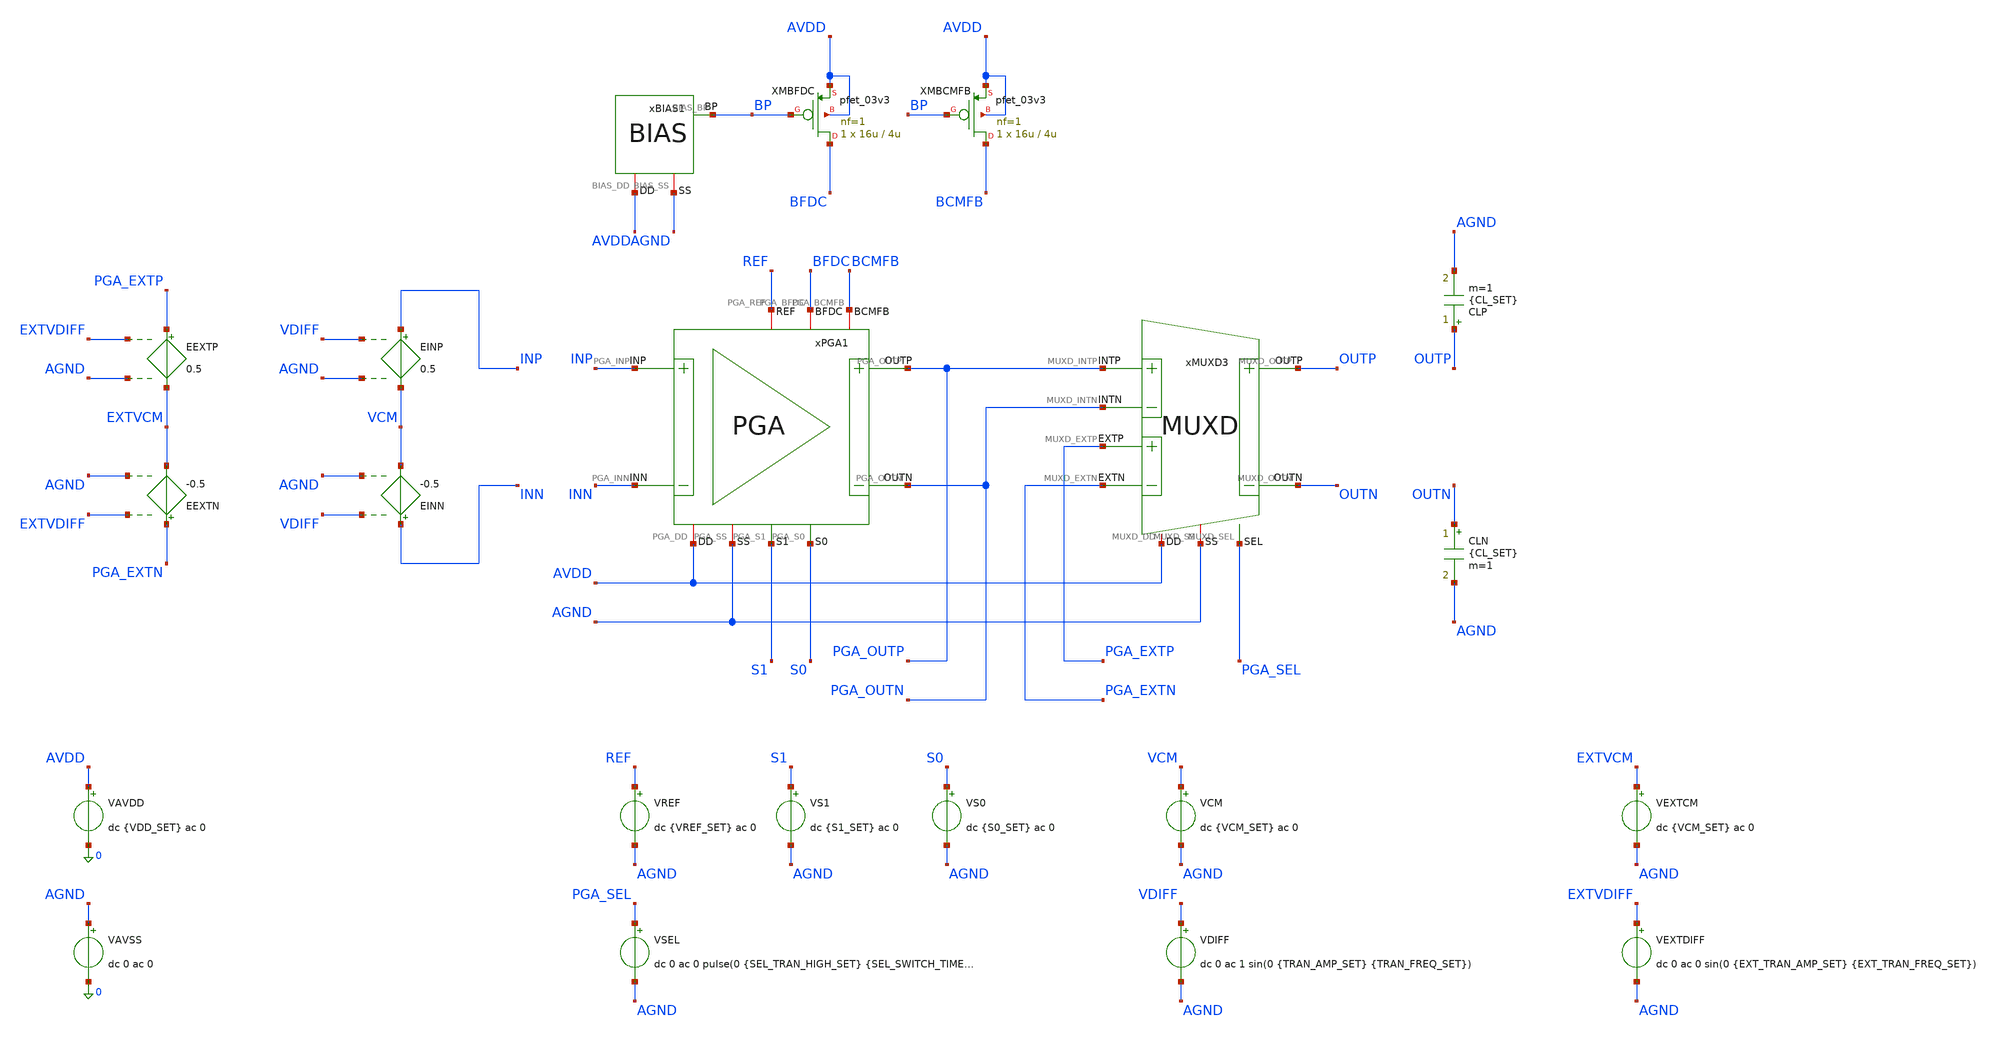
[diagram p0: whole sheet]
** sch_path: Design_Files/IC Design/Testbench/AFE_BLOCKS/PGA/PGA_TB_PVT_NOM.sch
**.subckt PGA_TB_PVT_NOM
CLP OUTP AGND {CL_SET} m=1
CLN OUTN AGND {CL_SET} m=1
xBIAS1 AVDD AGND BP BIAS
XMBFDC BFDC BP AVDD AVDD pfet_03v3 L=4u W=16u nf=1 ad='int((nf+1)/2) * W/nf * 0.18u' as='int((nf+2)/2) * W/nf * 0.18u'
+ pd='2*int((nf+1)/2) * (W/nf + 0.18u)' ps='2*int((nf+2)/2) * (W/nf + 0.18u)' nrd='0.18u / W' nrs='0.18u / W'
+ sa=0 sb=0 sd=0 m=1
XMBCMFB BCMFB BP AVDD AVDD pfet_03v3 L=4u W=16u nf=1 ad='int((nf+1)/2) * W/nf * 0.18u' as='int((nf+2)/2) * W/nf * 0.18u'
+ pd='2*int((nf+1)/2) * (W/nf + 0.18u)' ps='2*int((nf+2)/2) * (W/nf + 0.18u)' nrd='0.18u / W' nrs='0.18u / W'
+ sa=0 sb=0 sd=0 m=1
VAVDD AVDD 0 dc {VDD_SET} ac 0
.save i(vavdd)
VAVSS AGND 0 dc 0 ac 0
VCM VCM AGND dc {VCM_SET} ac 0
VDIFF VDIFF AGND dc 0 ac 1 sin(0 {TRAN_AMP_SET} {TRAN_FREQ_SET})
VREF REF AGND dc {VREF_SET} ac 0
VSEL PGA_SEL AGND dc 0 ac 0 pulse(0 {SEL_TRAN_HIGH_SET} {SEL_SWITCH_TIME_SET} 1u 1u 400m 800m)
VEXTCM EXTVCM AGND dc {VCM_SET} ac 0
VEXTDIFF EXTVDIFF AGND dc 0 ac 0 sin(0 {EXT_TRAN_AMP_SET} {EXT_TRAN_FREQ_SET})
EINP INP VCM VDIFF AGND 0.5
EINN INN VCM VDIFF AGND -0.5
EEXTP PGA_EXTP EXTVCM EXTVDIFF AGND 0.5
EEXTN PGA_EXTN EXTVCM EXTVDIFF AGND -0.5
xPGA1 AVDD AGND INP INN PGA_OUTN BFDC PGA_OUTP BCMFB REF S1 S0 PGA
xMUXD3 AVDD AGND PGA_OUTP PGA_OUTN OUTN OUTP PGA_EXTP PGA_EXTN PGA_SEL MUXD
VS1 S1 AGND dc {S1_SET} ac 0
VS0 S0 AGND dc {S0_SET} ac 0
**** begin user architecture code

* {MODELS_START}
.include $::180MCU_MODELS/design.ngspice

.param sw_stat_global=0
.param sw_stat_mismatch=0

.lib $::180MCU_MODELS/sm141064.ngspice typical
.lib $::180MCU_MODELS/sm141064.ngspice res_typical
.lib $::180MCU_MODELS/sm141064.ngspice mimcap_typical
.lib $::180MCU_MODELS/sm141064.ngspice cap_mim
.lib $::180MCU_MODELS/sm141064.ngspice bjt_typical

.csparam PROC_ID=0
* {MODELS_END}



* {SETUP_START}
.param VDD_SET=3.3
.param TEMP_SET=27

.param VCM_SET={VDD_SET/2}
.param VREF_SET={VDD_SET/2}

.param CL_SET=10p

.param S1_SET=0
.param S0_SET=0

.param PGA_G2_TARGET_SET=2
.param PGA_G4_TARGET_SET=4
.param PGA_G8_TARGET_SET=8
.param PGA_G16_TARGET_SET=16

.param TRAN_AMP_SET=50m
.param TRAN_FREQ_SET=10

.param EXT_TRAN_AMP_SET=0
.param EXT_TRAN_FREQ_SET=25

.param SEL_TRAN_HIGH_SET=0
.param SEL_SWITCH_TIME_SET=200m

.csparam MC_RUNS=200

.temp {TEMP_SET}

.options gmin=1e-12
.options rshunt=1e12
.options method=gear
* {SETUP_END}




* {MEAS_START}
.control

destroy all

set noaskquit
set wr_singlescale
unset wr_vecnames

option klu
option numdgt=15
option method=gear
option maxord=2
option plotwinsize=0

if $&PROC_ID = 0
set proc=NOM
else
if $&PROC_ID = 1
set proc=FF
else
if $&PROC_ID = 2
set proc=SS
else
if $&PROC_ID = 3
set proc=FS
else
set proc=SF
end
end
end
end

shell mkdir -p /foss/designs/ECG_Acquisition_IC/Measurement_Results/IC_Simulation/AFE_BLOCKS/PGA/{$proc}.Result_txt
shell rm -f /foss/designs/ECG_Acquisition_IC/Measurement_Results/IC_Simulation/AFE_BLOCKS/PGA/{$proc}.Result_txt/{$proc}.*.txt

foreach vddval 3.3 3.0 3.6
foreach tval 27 -40 125

if $vddval = 3.3
if $tval = 27
set env=nom
else
if $tval = -40
set env=tl
else
set env=th
end
end
else
if $vddval = 3.0
if $tval = 27
set env=vl
else
if $tval = -40
set env=vltl
else
set env=vlth
end
end
else
if $tval = 27
set env=vh
else
if $tval = -40
set env=vhtl
else
set env=vhth
end
end
end
end

alterparam VDD_SET=$vddval
alterparam TEMP_SET=$tval
alterparam SEL_TRAN_HIGH_SET=0
alterparam EXT_TRAN_AMP_SET=0

foreach gcode 0 1 2 3

if $gcode = 0
set gtag=g2
set gain_target=2
set s1v=0
set s0v=0
else
if $gcode = 1
set gtag=g4
set gain_target=4
set s1v=0
set s0v=$vddval
else
if $gcode = 2
set gtag=g8
set gain_target=8
set s1v=$vddval
set s0v=0
else
set gtag=g16
set gain_target=16
set s1v=$vddval
set s0v=$vddval
end
end
end

reset

alter @VS1[DC]=$s1v
alter @VS0[DC]=$s0v
alter @VSEL[DC]=0

alter @VDIFF[DC]=0

alter @VDIFF[ACMAG]=0
alter @VCM[ACMAG]=0
alter @VREF[ACMAG]=0
alter @VEXTDIFF[ACMAG]=0
alter @VAVDD[ACMAG]=0
alter @VAVSS[ACMAG]=0

save all
save @m.xmbfdc.m0[id]
save @m.xmbcmfb.m0[id]


* OFFSET

dc VDIFF -20m 20m 10u

let pga_diff=v(PGA_OUTP)-v(PGA_OUTN)

meas dc vos_meas when pga_diff=0 cross=1

set vos_val=$&vos_meas

echo $vos_val > /foss/designs/ECG_Acquisition_IC/Measurement_Results/IC_Simulation/AFE_BLOCKS/PGA/{$proc}.Result_txt/{$proc}.vos_{$gtag}_{$env}.txt

destroy all

alter @VDIFF[DC]=$vos_val


* OP

op

let op_index=0

let vdd=v(AVDD)-v(AGND)
let vref=v(REF)-v(AGND)

let vin_cm=0.5*(v(INP)+v(INN))-v(AGND)
let vin_diff=v(INP)-v(INN)

let pga_out_cm=0.5*(v(PGA_OUTP)+v(PGA_OUTN))-v(AGND)
let pga_out_diff=v(PGA_OUTP)-v(PGA_OUTN)
let pga_cm_error=pga_out_cm-vref

let out_cm=0.5*(v(OUTP)+v(OUTN))-v(AGND)
let out_diff=v(OUTP)-v(OUTN)

let idd_total=abs(vavdd#branch)
let power_total=vdd*idd_total

let ibfdc=abs(@m.xmbfdc.m0[id])
let ibcmfb=abs(@m.xmbcmfb.m0[id])

setscale op_index

wrdata /foss/designs/ECG_Acquisition_IC/Measurement_Results/IC_Simulation/AFE_BLOCKS/PGA/{$proc}.Result_txt/{$proc}.op_{$gtag}_{$env}.txt
+ vdd vref v(S1) v(S0) vin_cm vin_diff pga_out_cm pga_out_diff pga_cm_error out_cm out_diff idd_total power_total
+ ibfdc ibcmfb

destroy all


* DIFF AC

alter @VDIFF[ACMAG]=1
alter @VCM[ACMAG]=0
alter @VREF[ACMAG]=0
alter @VEXTDIFF[ACMAG]=0
alter @VAVDD[ACMAG]=0
alter @VAVSS[ACMAG]=0

ac dec 150 0.01 100Meg

let vin_diff=v(INP)-v(INN)
let pga_diff=v(PGA_OUTP)-v(PGA_OUTN)
let out_diff=v(OUTP)-v(OUTN)

let vin_r=real(vin_diff)
let vin_i=imag(vin_diff)

let pga_r=real(pga_diff)
let pga_i=imag(pga_diff)

let out_r=real(out_diff)
let out_i=imag(out_diff)

setscale frequency

wrdata /foss/designs/ECG_Acquisition_IC/Measurement_Results/IC_Simulation/AFE_BLOCKS/PGA/{$proc}.Result_txt/{$proc}.diff_ac_{$gtag}_{$env}.txt
+ vin_r vin_i pga_r pga_i out_r out_i

destroy all


* CMRR

alter @VDIFF[ACMAG]=0
alter @VCM[ACMAG]=1
alter @VREF[ACMAG]=0
alter @VEXTDIFF[ACMAG]=0
alter @VAVDD[ACMAG]=0
alter @VAVSS[ACMAG]=0

ac dec 100 0.01 1Meg

let vin_cm=0.5*(v(INP)+v(INN))-v(AGND)
let pga_diff=v(PGA_OUTP)-v(PGA_OUTN)

let vin_r=real(vin_cm)
let vin_i=imag(vin_cm)

let out_r=real(pga_diff)
let out_i=imag(pga_diff)

setscale frequency

wrdata /foss/designs/ECG_Acquisition_IC/Measurement_Results/IC_Simulation/AFE_BLOCKS/PGA/{$proc}.Result_txt/{$proc}.cmrr_ac_{$gtag}_{$env}.txt
+ vin_r vin_i out_r out_i

destroy all


* PSRR+

alter @VDIFF[ACMAG]=0
alter @VCM[ACMAG]=0
alter @VREF[ACMAG]=0
alter @VEXTDIFF[ACMAG]=0
alter @VAVDD[ACMAG]=1
alter @VAVDD[ACPHASE]=0
alter @VAVSS[ACMAG]=0

ac dec 100 0.01 1Meg

let vsup=v(AVDD)-v(AGND)
let pga_diff=v(PGA_OUTP)-v(PGA_OUTN)

let vsup_r=real(vsup)
let vsup_i=imag(vsup)

let out_r=real(pga_diff)
let out_i=imag(pga_diff)

setscale frequency

wrdata /foss/designs/ECG_Acquisition_IC/Measurement_Results/IC_Simulation/AFE_BLOCKS/PGA/{$proc}.Result_txt/{$proc}.psrrp_ac_{$gtag}_{$env}.txt
+ vsup_r vsup_i out_r out_i

destroy all


* PSRR-

alter @VDIFF[ACMAG]=0
alter @VCM[ACMAG]=0
alter @VREF[ACMAG]=0
alter @VEXTDIFF[ACMAG]=0
alter @VAVDD[ACMAG]=0
alter @VAVSS[ACMAG]=1
alter @VAVSS[ACPHASE]=0

ac dec 100 0.01 1Meg

let vsup=v(AVDD)-v(AGND)
let pga_diff=v(PGA_OUTP)-v(PGA_OUTN)

let vsup_r=real(vsup)
let vsup_i=imag(vsup)

let out_r=real(pga_diff)
let out_i=imag(pga_diff)

setscale frequency

wrdata /foss/designs/ECG_Acquisition_IC/Measurement_Results/IC_Simulation/AFE_BLOCKS/PGA/{$proc}.Result_txt/{$proc}.psrrn_ac_{$gtag}_{$env}.txt
+ vsup_r vsup_i out_r out_i

destroy all


* NOISE

alter @VDIFF[ACMAG]=1
alter @VCM[ACMAG]=0
alter @VREF[ACMAG]=0
alter @VEXTDIFF[ACMAG]=0
alter @VAVDD[ACMAG]=0
alter @VAVSS[ACMAG]=0

noise v(PGA_OUTP,PGA_OUTN) VDIFF dec 100 0.01 10k

setplot previous
setscale frequency

wrdata /foss/designs/ECG_Acquisition_IC/Measurement_Results/IC_Simulation/AFE_BLOCKS/PGA/{$proc}.Result_txt/{$proc}.noise_{$gtag}_{$env}.txt
+ onoise_spectrum inoise_spectrum

destroy all


* VTC

alter @VSEL[DC]=0
alter @VDIFF[DC]=0

alter @VDIFF[ACMAG]=0
alter @VCM[ACMAG]=0
alter @VREF[ACMAG]=0
alter @VEXTDIFF[ACMAG]=0
alter @VAVDD[ACMAG]=0
alter @VAVSS[ACMAG]=0

if $gcode = 0
let vtc_lim=1.2*$vddval/2
let vtc_step=2*$&vtc_lim/1000
dc VDIFF -$&vtc_lim $&vtc_lim $&vtc_step
end

if $gcode = 1
let vtc_lim=1.2*$vddval/4
let vtc_step=2*$&vtc_lim/1000
dc VDIFF -$&vtc_lim $&vtc_lim $&vtc_step
end

if $gcode = 2
let vtc_lim=1.2*$vddval/8
let vtc_step=2*$&vtc_lim/1000
dc VDIFF -$&vtc_lim $&vtc_lim $&vtc_step
end

if $gcode = 3
let vtc_lim=1.2*$vddval/16
let vtc_step=2*$&vtc_lim/1000
dc VDIFF -$&vtc_lim $&vtc_lim $&vtc_step
end

let vin_diff=v(INP)-v(INN)
let pga_outp=v(PGA_OUTP)-v(AGND)
let pga_outn=v(PGA_OUTN)-v(AGND)
let pga_out_cm=0.5*(v(PGA_OUTP)+v(PGA_OUTN))-v(AGND)
let pga_out_diff=v(PGA_OUTP)-v(PGA_OUTN)

wrdata /foss/designs/ECG_Acquisition_IC/Measurement_Results/IC_Simulation/AFE_BLOCKS/PGA/{$proc}.Result_txt/{$proc}.vtc_{$gtag}_{$env}.txt
+ vin_diff pga_outp pga_outn pga_out_cm pga_out_diff

destroy all


* THD

if $gcode = 0
alterparam TRAN_AMP_SET=0.60
end

if $gcode = 1
alterparam TRAN_AMP_SET=0.30
end

if $gcode = 2
alterparam TRAN_AMP_SET=0.15
end

if $gcode = 3
alterparam TRAN_AMP_SET=0.075
end

alterparam TRAN_FREQ_SET=60

reset

alter @VS1[DC]=$s1v
alter @VS0[DC]=$s0v
alter @VSEL[DC]=0
alter @VDIFF[DC]=0

alter @VDIFF[ACMAG]=0
alter @VCM[ACMAG]=0
alter @VREF[ACMAG]=0
alter @VEXTDIFF[ACMAG]=0
alter @VAVDD[ACMAG]=0
alter @VAVSS[ACMAG]=0

save v(INP) v(INN)
save v(PGA_OUTP) v(PGA_OUTN)

tran 50u 266.666667m 100m

let vin_diff=v(INP)-v(INN)
let pga_out_diff=v(PGA_OUTP)-v(PGA_OUTN)

wrdata /foss/designs/ECG_Acquisition_IC/Measurement_Results/IC_Simulation/AFE_BLOCKS/PGA/{$proc}.Result_txt/{$proc}.thd_{$gtag}_{$env}.txt
+ vin_diff pga_out_diff

destroy all

alterparam TRAN_AMP_SET=50m
alterparam TRAN_FREQ_SET=10

end

end
end


* SEL FUNCTIONAL

if $&PROC_ID = 0

alterparam VDD_SET=3.3
alterparam TEMP_SET=27

alterparam TRAN_AMP_SET=50m
alterparam TRAN_FREQ_SET=10

alterparam EXT_TRAN_AMP_SET=50m
alterparam EXT_TRAN_FREQ_SET=25

alterparam SEL_TRAN_HIGH_SET=3.3
alterparam SEL_SWITCH_TIME_SET=200m

reset

alter @VS1[DC]=0
alter @VS0[DC]=0

save all

tran 20u 400m

let int_diff=v(PGA_OUTP)-v(PGA_OUTN)
let ext_diff=v(PGA_EXTP)-v(PGA_EXTN)
let out_diff=v(OUTP)-v(OUTN)

wrdata /foss/designs/ECG_Acquisition_IC/Measurement_Results/IC_Simulation/AFE_BLOCKS/PGA/{$proc}.Result_txt/{$proc}.sel_tran_nom.txt
+ v(PGA_SEL) int_diff ext_diff out_diff

destroy all

end


* GAIN SWITCH FUNCTIONAL

if $&PROC_ID = 0

alterparam VDD_SET=3.3
alterparam TEMP_SET=27

alterparam TRAN_AMP_SET=50m
alterparam TRAN_FREQ_SET=10

alterparam EXT_TRAN_AMP_SET=0
alterparam SEL_TRAN_HIGH_SET=0

reset

alter @VS1[DC]=0
alter @VS0[DC]=0
alter @VSEL[DC]=0

compose S1PWL values 0 0 199.98m 0 200m 3.3 400m 3.3

compose S0PWL values 0 0 99.98m 0 100m 3.3 199.98m 3.3 200m 0 299.98m 0 300m 3.3 400m 3.3

alter @VS1[pwl]=S1PWL
alter @VS0[pwl]=S0PWL

save all

tran 20u 400m

let vin_diff=v(INP)-v(INN)
let pga_diff=v(PGA_OUTP)-v(PGA_OUTN)

setscale time

wrdata /foss/designs/ECG_Acquisition_IC/Measurement_Results/IC_Simulation/AFE_BLOCKS/PGA/{$proc}.Result_txt/{$proc}.gain_switch_tran_nom.txt
+ v(S1) v(S0) vin_diff pga_diff

destroy all

end

quit

.endc
* {MEAS_END}


**** end user architecture code
**.ends
.end
